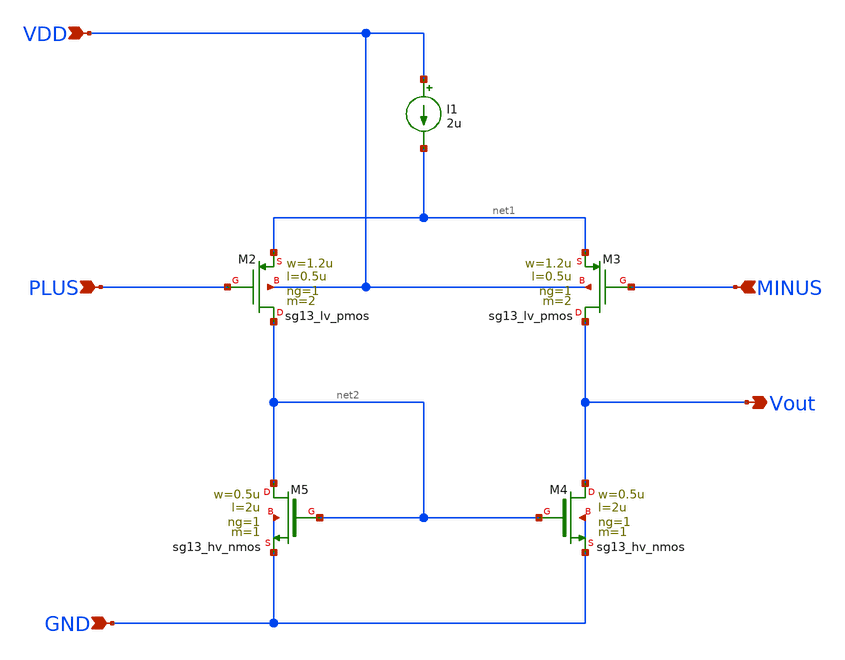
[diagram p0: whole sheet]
** sch_path: Design Files/RAMP/OTA/POTA.sch
**.subckt POTA VDD GND PLUS MINUS Vout
*.ipin VDD
*.ipin GND
*.ipin PLUS
*.ipin MINUS
*.opin Vout
XM2 net2 PLUS net1 VDD sg13_lv_pmos w=1.2u l=0.5u ng=1 m=2 mm_ok=1
XM3 Vout MINUS net1 VDD sg13_lv_pmos w=1.2u l=0.5u ng=1 m=2 mm_ok=1
XM4 Vout net2 GND GND sg13_hv_nmos w=0.5u l=2u ng=1 m=1 mm_ok=1
XM5 net2 net2 GND GND sg13_hv_nmos w=0.5u l=2u ng=1 m=1 mm_ok=1
I1 VDD net1 2u
**.ends
.end
